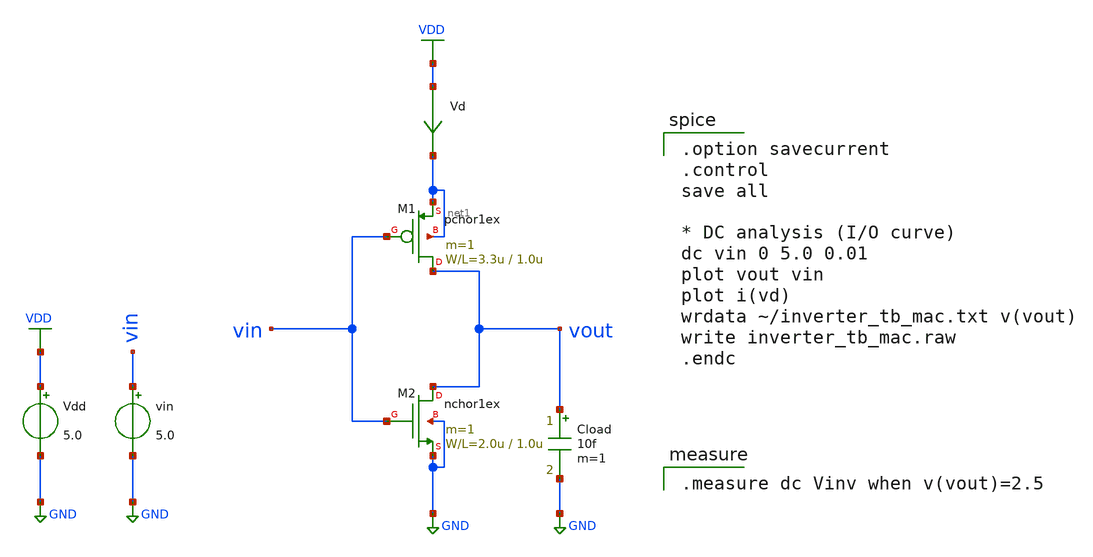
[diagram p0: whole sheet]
** sch_path: samples/inverter/PTS06/inverter_tb_mac.sch
**.subckt inverter_tb_mac
Vdd VDD GND 5.0
vin vin GND 5.0
Vd VDD net1 0
.save i(vd)
Cload vout GND 10f m=1
M1 vout vin net1 net1 pchor1ex L=1.0u W=3.3u m=1
M2 vout vin GND GND nchor1ex L=1.0u W=2.0u m=1
**** begin user architecture code
 .include /Users/[user]/.xschem/lib/PTS06/mos.lib
.include /Users/[user]/.xschem/lib/PTS06/stdcells.lib

.option savecurrent
.control
save all

* DC analysis (I/O curve)
dc vin 0 5.0 0.01
plot vout vin
plot i(vd)
wrdata ~/inverter_tb_mac.txt v(vout)
write inverter_tb_mac.raw
.endc


.measure dc Vinv when v(vout)=2.5

**** end user architecture code
**.ends
.GLOBAL VDD
.GLOBAL GND
.end
